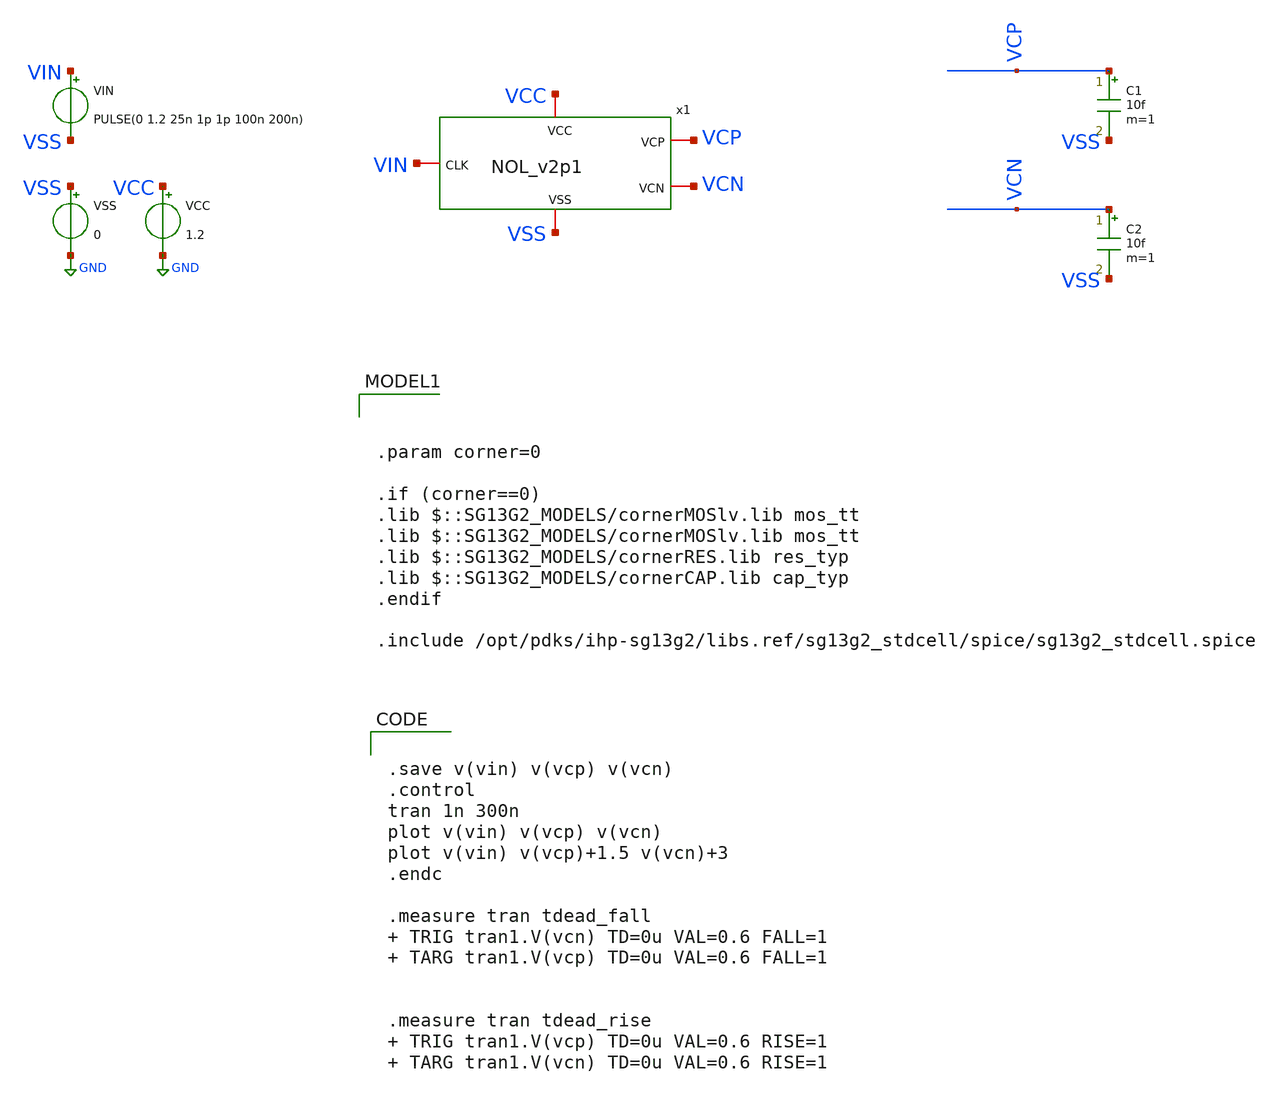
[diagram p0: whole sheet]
** sch_path: xschem/tb_NOL_reportslack.sch
**.subckt tb_NOL_reportslack
VCC VCC GND 1.2
VSS VSS GND 0
VIN VIN VSS PULSE(0 1.2 25n 1p 1p 100n 200n)
C1 VCP VSS 10f m=1
C2 VCN VSS 10f m=1
x1 VCC VSS VCP VIN VCN NOL_v2p1
**** begin user architecture code


.save v(vin) v(vcp) v(vcn)
.control
tran 1n 300n
plot v(vin) v(vcp) v(vcn)
plot v(vin) v(vcp)+1.5 v(vcn)+3
.endc

.measure tran tdead_fall  TRIG tran1.V(vcn) TD=0u VAL=0.6 FALL=1  TARG tran1.V(vcp) TD=0u VAL=0.6
+ FALL=1


.measure tran tdead_rise  TRIG tran1.V(vcp) TD=0u VAL=0.6 RISE=1  TARG tran1.V(vcn) TD=0u VAL=0.6
+ RISE=1






.param corner=0

.if (corner==0)
.lib $::SG13G2_MODELS/cornerMOSlv.lib mos_tt
.lib $::SG13G2_MODELS/cornerMOSlv.lib mos_tt
.lib $::SG13G2_MODELS/cornerRES.lib res_typ
.lib $::SG13G2_MODELS/cornerCAP.lib cap_typ
.endif

.include /opt/pdks/ihp-sg13g2/libs.ref/sg13g2_stdcell/spice/sg13g2_stdcell.spice

**** end user architecture code
**.ends
.GLOBAL GND
.end
